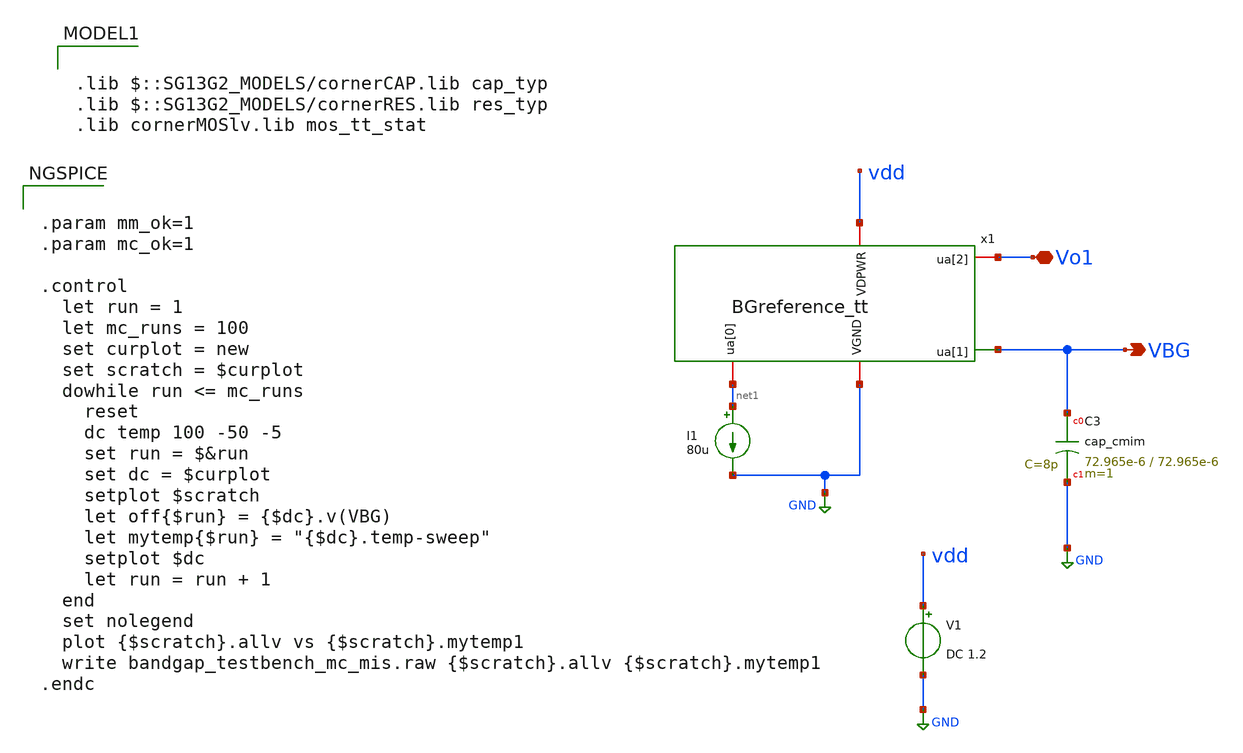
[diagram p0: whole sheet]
** sch_path: Tapeout/bandgap_MC_test.sch
**.subckt bandgap_MC_test VBG Vo1
*.opin VBG
*.iopin Vo1
V1 vdd GND DC 1.2
I1 net1 GND 80u
XC3 VBG GND cap_cmim w=72.965e-6 l=72.965e-6 m=1 mm_ok=1
x1 vdd net1 Vo1 GND VBG BGreference_tt
**** begin user architecture code


.param mm_ok=1
.param mc_ok=1

.control
  let run = 1
  let mc_runs = 100
  set curplot = new
  set scratch = $curplot
  dowhile run <= mc_runs
    reset
    dc temp 100 -50 -5
    set run = $&run
    set dc = $curplot
    setplot $scratch
    let off{$run} = {$dc}.v(VBG)
    let mytemp{$run} = "{$dc}.temp-sweep"
    setplot $dc
    let run = run + 1
  end
  set nolegend
  plot {$scratch}.allv vs {$scratch}.mytemp1
  write bandgap_testbench_mc_mis.raw {$scratch}.allv {$scratch}.mytemp1
.endc




.lib $::SG13G2_MODELS/cornerCAP.lib cap_typ
.lib $::SG13G2_MODELS/cornerRES.lib res_typ
.lib cornerMOSlv.lib mos_tt_stat
**** end user architecture code
**.ends

* expanding   symbol:  /foss/designs/simulations/tiny_tapeout_final/BGreference_tt.sym # of pins=5
** sym_path: Tapeout/BGreference_tt.sym
** sch_path: Tapeout/BGreference_tt.sch
.subckt BGreference_tt VDPWR ua[0] ua[2] VGND ua[1]
*.opin ua[1]
*.iopin VGND
*.iopin VDPWR
*.iopin ua[0]
*.iopin ua[2]
XM8 VGND v- net1 sub! sg13_lv_nmos w=150n l=10u ng=1 m=1 mm_ok=1
XM6 net1 net1 VDPWR bulk6 sg13_lv_pmos w=1u l=1u ng=1 m=1 mm_ok=1
XM7 net2 net1 VDPWR bulk6 sg13_lv_pmos w=1u l=1u ng=1 m=1 mm_ok=1
XM9 v- net2 VDPWR bulk5 sg13_lv_pmos w=200n l=4u ng=1 m=1 mm_ok=1
XM1 v- v+ VGND sub! sg13_lv_nmos w=7.14u l=5u ng=4 m=1 mm_ok=1
XM2 net3 net3 VGND sub! sg13_lv_nmos w=21u l=5u ng=8 m=1 mm_ok=1
XM3 v- ua[2] VDPWR bulk7 sg13_lv_pmos w=15u l=5u ng=8 m=1 mm_ok=1
XM4 v+ ua[2] VDPWR bulk7 sg13_lv_pmos w=15u l=5u ng=8 m=1 mm_ok=1
XM5 ua[1] ua[2] VDPWR bulk7 sg13_lv_pmos w=16u l=5u ng=8 m=1 mm_ok=1
XR2 ua[1] net11 sub! rppd w=0.710e-6 l=38.65e-6 m=1 b=0 mm_ok=1
XC1 net2 VGND cap_cmim w=18.2e-6 l=18.2e-6 m=1 mm_ok=1
XM10 dn3 v- dn2 bulk sg13_lv_pmos w=3.64u l=3.7u ng=1 m=2 mm_ok=1
XM11 dn4 v+ dn2 bulk sg13_lv_pmos w=3.64u l=3.7u ng=1 m=2 mm_ok=1
XM12 dn4 VDPWR VDPWR bulk sg13_lv_pmos w=3.64u l=3.7u ng=1 m=2 mm_ok=1
XM13 dn3 VDPWR VDPWR bulk sg13_lv_pmos w=3.64u l=3.7u ng=1 m=2 mm_ok=1
XM15 dn2 VDPWR VDPWR bulk sg13_lv_pmos w=3.64u l=3.7u ng=1 m=2 mm_ok=1
XM16 dn2 VDPWR VDPWR bulk sg13_lv_pmos w=3.64u l=3.7u ng=1 m=2 mm_ok=1
XR4 VDPWR bulk ntap1 R=262.8 w=0.78e-6 l=0.78e-6
XM14 dn2 ua[0] VDPWR bulk1 sg13_lv_pmos w=5.3u l=1.95u ng=1 m=1 mm_ok=1
XR5 VGND sub! ptap1 R=30.62 w=10e-6 l=1.0e-6
XR6 VDPWR bulk1 ntap1 R=262.8 w=0.78e-6 l=0.78e-6
XM17 VGND dn3 dn3 sub! sg13_lv_nmos w=720n l=9.75u ng=1 m=1 mm_ok=1
XM18 VGND dn3 dn4 sub! sg13_lv_nmos w=720n l=9.75u ng=1 m=1 mm_ok=1
XM19 ua[2] ua[0] VDPWR bulk4 sg13_lv_pmos w=75u l=2.08u ng=8 m=1 mm_ok=1
XM20 VGND dn4 ua[2] sub! sg13_lv_nmos w=28.8u l=9.75u ng=4 m=1 mm_ok=1
XM21 ua[0] ua[0] VDPWR bulk4 sg13_lv_pmos w=75u l=2.08u ng=8 m=1 mm_ok=1
XC2 dn4 ua[2] cap_cmim w=22.29e-6 l=22.29e-6 m=1 mm_ok=1
XR8 VDPWR bulk4 ntap1 R=262.8 w=0.78e-6 l=0.78e-6
XR9 VDPWR bulk6 ntap1 R=262.8 w=0.78e-6 l=0.78e-6
XR12 v+ net7 sub! rppd w=0.5e-6 l=38.65e-6 m=1 b=0 mm_ok=1
XR3 net7 net6 sub! rppd w=0.5e-6 l=38.65e-6 m=1 b=0 mm_ok=1
XR13 net6 net5 sub! rppd w=0.5e-6 l=38.65e-6 m=1 b=0 mm_ok=1
XR14 net5 net4 sub! rppd w=0.5e-6 l=38.65e-6 m=1 b=0 mm_ok=1
XR15 net4 net3 sub! rppd w=0.5e-6 l=38.65e-6 m=1 b=0 mm_ok=1
XR16 net10 net9 sub! rppd w=0.5e-6 l=38.65e-6 m=1 b=0 mm_ok=1
XR17 net9 net8 sub! rppd w=0.5e-6 l=38.65e-6 m=1 b=0 mm_ok=1
XR18 net8 net17 sub! rppd w=0.5e-6 l=38.65e-6 m=1 b=0 mm_ok=1
XR19 net17 VGND sub! rppd w=3e-6 l=38.65e-6 m=1 b=0 mm_ok=1
XR20 net11 net12 sub! rppd w=0.710e-6 l=38.65e-6 m=1 b=0 mm_ok=1
XR21 net12 net13 sub! rppd w=0.710e-6 l=38.65e-6 m=1 b=0 mm_ok=1
XR22 net13 net14 sub! rppd w=0.710e-6 l=38.65e-6 m=1 b=0 mm_ok=1
XR23 net14 net15 sub! rppd w=0.710e-6 l=38.65e-6 m=1 b=0 mm_ok=1
XR24 net15 net16 sub! rppd w=0.710e-6 l=38.65e-6 m=1 b=0 mm_ok=1
XR25 net16 VGND sub! rppd w=0.710e-6 l=38.65e-6 m=1 b=0 mm_ok=1
XR26 VDPWR bulk5 ntap1 R=262.8 w=0.78e-6 l=0.78e-6
XR27 VDPWR bulk7 ntap1 R=262.8 w=0.78e-6 l=0.78e-6
XC3 VDPWR VGND cap_cmim w=5e-6 l=5e-6 m=15 mm_ok=1
XR31 v+ net10 sub! rppd w=0.5e-6 l=38.65e-6 m=1 b=0 mm_ok=1
.ends

.GLOBAL GND
.end
